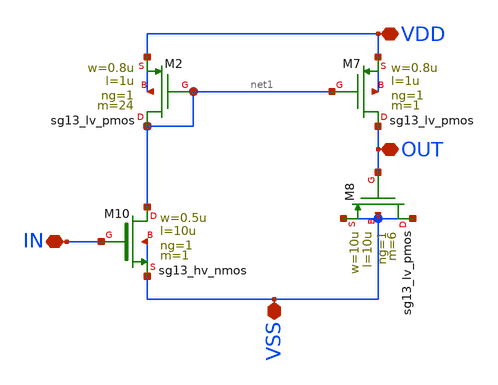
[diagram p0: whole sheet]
** sch_path: xschem/Delay.sch
**.subckt Delay VDD OUT VSS IN
*.iopin VDD
*.iopin OUT
*.iopin VSS
*.iopin IN
XM7 OUT net1 VDD VDD sg13_lv_pmos w=0.8u l=1u ng=1 m=1 mm_ok=1
XM8 VSS OUT VSS VSS sg13_lv_pmos w=10u l=10u ng=1 m=6 mm_ok=1
XM10 net1 IN VSS VSS sg13_hv_nmos w=0.5u l=10u ng=1 m=1 mm_ok=1
XM2 net1 net1 VDD VDD sg13_lv_pmos w=0.8u l=1u ng=1 m=24 mm_ok=1
**.ends
.end
